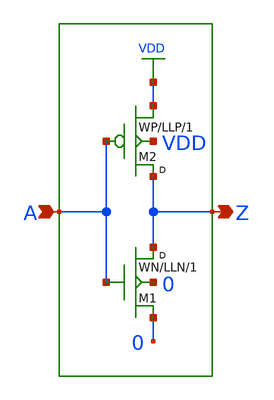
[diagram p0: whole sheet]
** sch_path: xschem_library/examples/cmos_inv.sch
**.subckt cmos_inv A Z
*.ipin A
*.opin Z
M1 Z A 0 0 n w=WN l=LLN m=1
M2 Z A VDD VDD p w=WP l=LLP m=1
**.ends
.GLOBAL VDD
.end
